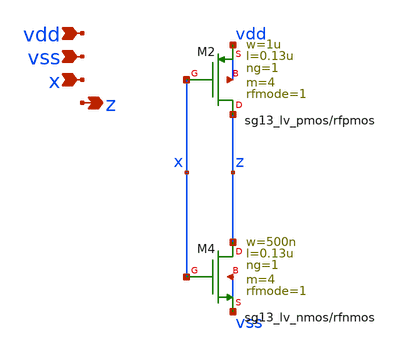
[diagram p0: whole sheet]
** sch_path: MSPHY9932-main/sch/buf_4.sch
**.subckt buf_4 vdd vss x z
*.ipin vdd
*.ipin vss
*.ipin x
*.opin z
XM2 z x vdd vdd sg13_lv_pmos w=1u l=0.13u ng=1 m=4 rfmode=1 mm_ok=1
XM4 z x vss vss sg13_lv_nmos w=500n l=0.13u ng=1 m=4 rfmode=1 mm_ok=1
**.ends
.end
